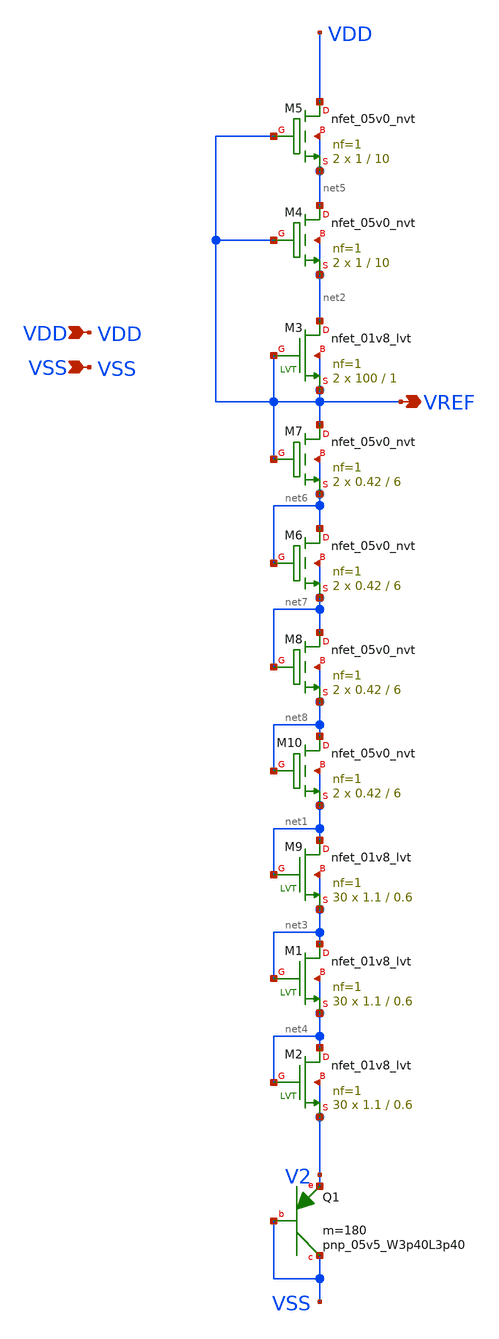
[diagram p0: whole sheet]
** sch_path: design/LELO_SVOD_SKY130A/LELO_SVOD_VTREF.sch
**.subckt LELO_SVOD_VTREF VDD VSS VREF
*.ipin VDD
*.ipin VSS
*.opin VREF
XQ1 VSS VSS V2 sky130_fd_pr__pnp_05v5_W3p40L3p40 m=180
XM3 net2 VREF VREF VREF sky130_fd_pr__nfet_01v8_lvt L=1 W=100 nf=1 ad='int((1 + 1)/2) * 100 / 1 * 0.29'
+ as='int((1 + 2)/2) * 100 / 1 * 0.29' pd='2*int((1 + 1)/2) * (100 / 1 + 0.29)' ps='2*int((1 + 2)/2) * (100 / 1 + 0.29)'
+ nrd='0.29 / 100 ' nrs='0.29 / 100 ' sa=0 sb=0 sd=0 mult=2 m=2
XM9 net1 net1 net3 net3 sky130_fd_pr__nfet_01v8_lvt L=0.6 W=1.1 nf=1 ad='int((1 + 1)/2) * 1.1 / 1 * 0.29'
+ as='int((1 + 2)/2) * 1.1 / 1 * 0.29' pd='2*int((1 + 1)/2) * (1.1 / 1 + 0.29)' ps='2*int((1 + 2)/2) * (1.1 / 1 + 0.29)'
+ nrd='0.29 / 1.1 ' nrs='0.29 / 1.1 ' sa=0 sb=0 sd=0 mult=30 m=30
XM1 net3 net3 net4 net4 sky130_fd_pr__nfet_01v8_lvt L=0.6 W=1.1 nf=1 ad='int((1 + 1)/2) * 1.1 / 1 * 0.29'
+ as='int((1 + 2)/2) * 1.1 / 1 * 0.29' pd='2*int((1 + 1)/2) * (1.1 / 1 + 0.29)' ps='2*int((1 + 2)/2) * (1.1 / 1 + 0.29)'
+ nrd='0.29 / 1.1 ' nrs='0.29 / 1.1 ' sa=0 sb=0 sd=0 mult=30 m=30
XM2 net4 net4 V2 V2 sky130_fd_pr__nfet_01v8_lvt L=0.6 W=1.1 nf=1 ad='int((1 + 1)/2) * 1.1 / 1 * 0.29'
+ as='int((1 + 2)/2) * 1.1 / 1 * 0.29' pd='2*int((1 + 1)/2) * (1.1 / 1 + 0.29)' ps='2*int((1 + 2)/2) * (1.1 / 1 + 0.29)'
+ nrd='0.29 / 1.1 ' nrs='0.29 / 1.1 ' sa=0 sb=0 sd=0 mult=30 m=30
XM4 net5 VREF net2 net2 sky130_fd_pr__nfet_05v0_nvt L=10 W=1 nf=1 ad='int((1 + 1)/2) * 1 / 1 * 0.29'
+ as='int((1 + 2)/2) * 1 / 1 * 0.29' pd='2*int((1 + 1)/2) * (1 / 1 + 0.29)' ps='2*int((1 + 2)/2) * (1 / 1 + 0.29)'
+ nrd='0.29 / 1 ' nrs='0.29 / 1 ' sa=0 sb=0 sd=0 mult=2 m=2
XM5 VDD VREF net5 net5 sky130_fd_pr__nfet_05v0_nvt L=10 W=1 nf=1 ad='int((1 + 1)/2) * 1 / 1 * 0.29' as='int((1 + 2)/2) * 1 / 1 * 0.29'
+ pd='2*int((1 + 1)/2) * (1 / 1 + 0.29)' ps='2*int((1 + 2)/2) * (1 / 1 + 0.29)' nrd='0.29 / 1 ' nrs='0.29 / 1 '
+ sa=0 sb=0 sd=0 mult=2 m=2
XM7 VREF VREF net6 net6 sky130_fd_pr__nfet_05v0_nvt L=6 W=0.42 nf=1 ad='int((1 + 1)/2) * 0.42 / 1 * 0.29'
+ as='int((1 + 2)/2) * 0.42 / 1 * 0.29' pd='2*int((1 + 1)/2) * (0.42 / 1 + 0.29)' ps='2*int((1 + 2)/2) * (0.42 / 1 + 0.29)'
+ nrd='0.29 / 0.42 ' nrs='0.29 / 0.42 ' sa=0 sb=0 sd=0 mult=2 m=2
XM6 net6 net6 net7 net7 sky130_fd_pr__nfet_05v0_nvt L=6 W=0.42 nf=1 ad='int((1 + 1)/2) * 0.42 / 1 * 0.29'
+ as='int((1 + 2)/2) * 0.42 / 1 * 0.29' pd='2*int((1 + 1)/2) * (0.42 / 1 + 0.29)' ps='2*int((1 + 2)/2) * (0.42 / 1 + 0.29)'
+ nrd='0.29 / 0.42 ' nrs='0.29 / 0.42 ' sa=0 sb=0 sd=0 mult=2 m=2
XM8 net7 net7 net8 net8 sky130_fd_pr__nfet_05v0_nvt L=6 W=0.42 nf=1 ad='int((1 + 1)/2) * 0.42 / 1 * 0.29'
+ as='int((1 + 2)/2) * 0.42 / 1 * 0.29' pd='2*int((1 + 1)/2) * (0.42 / 1 + 0.29)' ps='2*int((1 + 2)/2) * (0.42 / 1 + 0.29)'
+ nrd='0.29 / 0.42 ' nrs='0.29 / 0.42 ' sa=0 sb=0 sd=0 mult=2 m=2
XM10 net8 net8 net1 net1 sky130_fd_pr__nfet_05v0_nvt L=6 W=0.42 nf=1 ad='int((1 + 1)/2) * 0.42 / 1 * 0.29'
+ as='int((1 + 2)/2) * 0.42 / 1 * 0.29' pd='2*int((1 + 1)/2) * (0.42 / 1 + 0.29)' ps='2*int((1 + 2)/2) * (0.42 / 1 + 0.29)'
+ nrd='0.29 / 0.42 ' nrs='0.29 / 0.42 ' sa=0 sb=0 sd=0 mult=2 m=2
**.ends
.end
